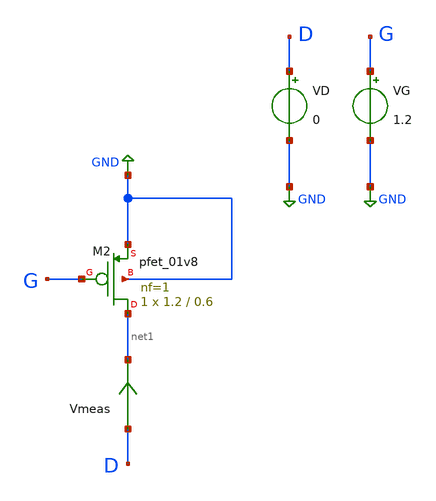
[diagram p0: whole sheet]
** sch_path: nmos-pmos/pmos1.sch
**.subckt pmos1
VD D GND 0
VG G GND 1.2
Vmeas D net1 0
.save i(vmeas)
XM2 net1 G GND GND sky130_fd_pr__pfet_01v8 L=0.6 W=1.2 nf=1 ad='int((nf+1)/2) * W/nf * 0.29' as='int((nf+2)/2) * W/nf * 0.29'
+ pd='2*int((nf+1)/2) * (W/nf + 0.29)' ps='2*int((nf+2)/2) * (W/nf + 0.29)' nrd='0.29 / W' nrs='0.29 / W'
+ sa=0 sb=0 sd=0 mult=1 m=1
**** begin user architecture code


.lib /foss/pdk/sky130A/libs.tech/ngspice/sky130.lib.spice tt

.control
   dc VD 0 -3 -0.2 VG 0 -3 -0.2
   plot -i(VD)

.endc

.save all


**** end user architecture code
**.ends
.GLOBAL GND
.end
